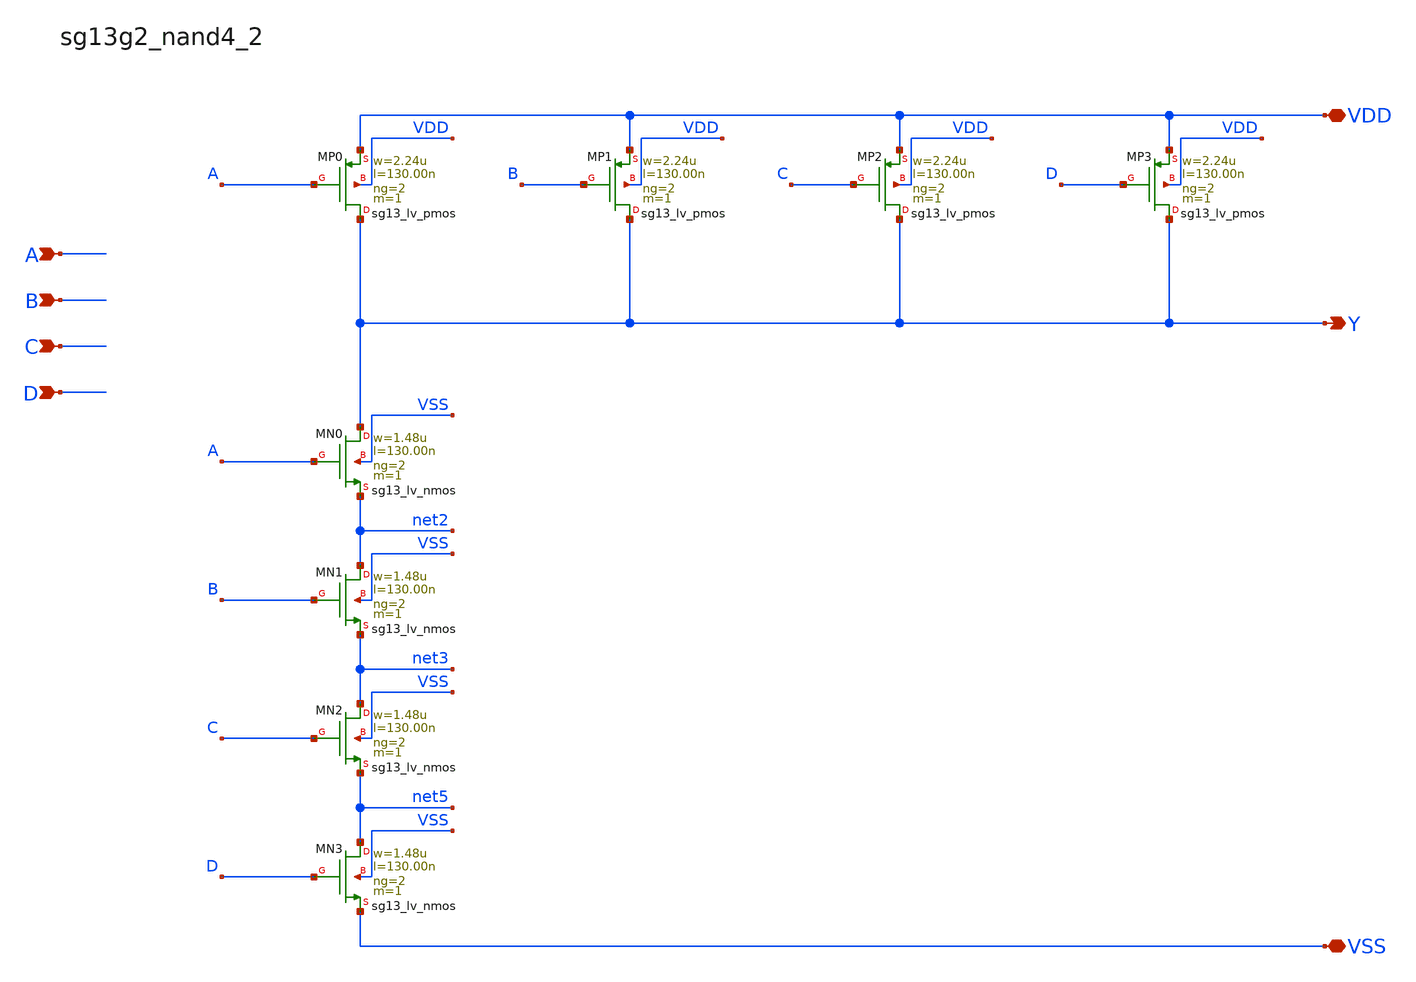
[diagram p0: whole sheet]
** sch_path: outputs/sg13g2_cells/cells/sg13g2_nand4_2/sg13g2_nand4_2.sch
**.subckt sg13g2_nand4_2 Y A B C D VDD VSS
*.opin Y
*.ipin A
*.ipin B
*.ipin C
*.ipin D
*.iopin VDD
*.iopin VSS
XMP3 Y D VDD VDD sg13_lv_pmos w=2.24u l=130.00n ng=2 m=1 mm_ok=1
XMP0 Y A VDD VDD sg13_lv_pmos w=2.24u l=130.00n ng=2 m=1 mm_ok=1
XMP1 Y B VDD VDD sg13_lv_pmos w=2.24u l=130.00n ng=2 m=1 mm_ok=1
XMP2 Y C VDD VDD sg13_lv_pmos w=2.24u l=130.00n ng=2 m=1 mm_ok=1
XMN1 net2 B net3 VSS sg13_lv_nmos w=1.48u l=130.00n ng=2 m=1 mm_ok=1
XMN2 net3 C net5 VSS sg13_lv_nmos w=1.48u l=130.00n ng=2 m=1 mm_ok=1
XMN0 Y A net2 VSS sg13_lv_nmos w=1.48u l=130.00n ng=2 m=1 mm_ok=1
XMN3 net5 D VSS VSS sg13_lv_nmos w=1.48u l=130.00n ng=2 m=1 mm_ok=1
**.ends
.end
